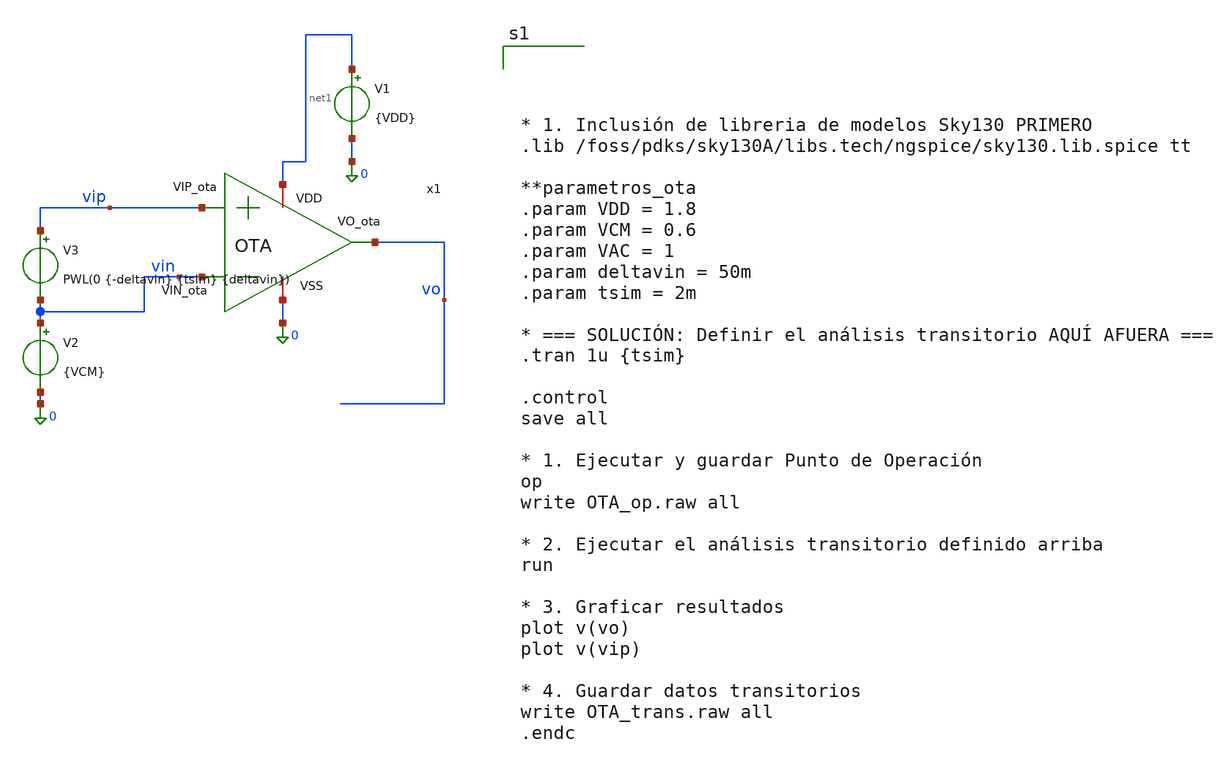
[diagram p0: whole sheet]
** sch_path: xschem/OTA_tbtran.sch
**.subckt OTA_tbtran
x1 net1 vo vin vip 0 OTA
V1 net1 0 {VDD}
V2 vin 0 {VCM}
V3 vip vin PWL(0 {-deltavin} {tsim} {deltavin})
**** begin user architecture code




* 1. Inclusión de libreria de modelos Sky130 PRIMERO
.lib /foss/pdks/sky130A/libs.tech/ngspice/sky130.lib.spice tt

**parametros_ota
.param VDD = 1.8
.param VCM = 0.6
.param VAC = 1
.param deltavin = 50m
.param tsim = 2m

* === SOLUCIÓN: Definir el análisis transitorio AQUÍ AFUERA ===
.tran 1u {tsim}

.control
save all

* 1. Ejecutar y guardar Punto de Operación
op
write OTA_op.raw all

* 2. Ejecutar el análisis transitorio definido arriba
run

* 3. Graficar resultados
plot v(vo)
plot v(vip)

* 4. Guardar datos transitorios
write OTA_trans.raw all
.endc



**** end user architecture code
**.ends

* expanding   symbol:  /foss/designs/LDO-sky130/xschem/OTA.sym # of pins=5
** sym_path: xschem/OTA.sym
** sch_path: xschem/OTA.sch
.subckt OTA VDD VO_ota VIN_ota VIP_ota VSS
*.ipin VIN_ota
*.opin VO_ota
*.iopin VSS
*.iopin VDD
*.ipin VIP_ota
XR1 VO_ota1 net1 VDD sky130_fd_pr__res_high_po W=0.35 L=360 mult=1 m=1
XC1 VO_ota net1 sky130_fd_pr__cap_mim_m3_2 W=50 L=50 MF=1 m=1
XMpr VO_ota1 vd VSS VSS sky130_fd_pr__nfet_01v8 L=0.5 W=3 nf=1 ad='int((1 + 1)/2) * 3 / 1 * 0.29' as='int((1 + 2)/2) * 3 / 1 * 0.29'
+ pd='2*int((1 + 1)/2) * (3 / 1 + 0.29)' ps='2*int((1 + 2)/2) * (3 / 1 + 0.29)' nrd='0.29 / 3 ' nrs='0.29 / 3 '
+ sa=0 sb=0 sd=0 mult=1 m=1
XMnr vd vd VSS VSS sky130_fd_pr__nfet_01v8 L=0.5 W=3 nf=1 ad='int((1 + 1)/2) * 3 / 1 * 0.29' as='int((1 + 2)/2) * 3 / 1 * 0.29'
+ pd='2*int((1 + 1)/2) * (3 / 1 + 0.29)' ps='2*int((1 + 2)/2) * (3 / 1 + 0.29)' nrd='0.29 / 3 ' nrs='0.29 / 3 '
+ sa=0 sb=0 sd=0 mult=1 m=1
XMn vd VIN_ota Vtail VDD sky130_fd_pr__pfet_01v8 L=0.5 W=28 nf=1 ad='int((1 + 1)/2) * 28 / 1 * 0.29'
+ as='int((1 + 2)/2) * 28 / 1 * 0.29' pd='2*int((1 + 1)/2) * (28 / 1 + 0.29)' ps='2*int((1 + 2)/2) * (28 / 1 + 0.29)'
+ nrd='0.29 / 28 ' nrs='0.29 / 28 ' sa=0 sb=0 sd=0 mult=1 m=1
XMp VO_ota1 VIP_ota Vtail VDD sky130_fd_pr__pfet_01v8 L=0.5 W=28 nf=1 ad='int((1 + 1)/2) * 28 / 1 * 0.29'
+ as='int((1 + 2)/2) * 28 / 1 * 0.29' pd='2*int((1 + 1)/2) * (28 / 1 + 0.29)' ps='2*int((1 + 2)/2) * (28 / 1 + 0.29)'
+ nrd='0.29 / 28 ' nrs='0.29 / 28 ' sa=0 sb=0 sd=0 mult=1 m=1
XMo VO_ota VO_ota1 VSS VSS sky130_fd_pr__nfet_01v8 L=0.5 W=3 nf=1 ad='int((1 + 1)/2) * 3 / 1 * 0.29'
+ as='int((1 + 2)/2) * 3 / 1 * 0.29' pd='2*int((1 + 1)/2) * (3 / 1 + 0.29)' ps='2*int((1 + 2)/2) * (3 / 1 + 0.29)'
+ nrd='0.29 / 3 ' nrs='0.29 / 3 ' sa=0 sb=0 sd=0 mult=1 m=1
XMrc1 Vtail VGP VDD VDD sky130_fd_pr__pfet_01v8_lvt L=0.5 W=40 nf=1 ad='int((1 + 1)/2) * 40 / 1 * 0.29'
+ as='int((1 + 2)/2) * 40 / 1 * 0.29' pd='2*int((1 + 1)/2) * (40 / 1 + 0.29)' ps='2*int((1 + 2)/2) * (40 / 1 + 0.29)'
+ nrd='0.29 / 40 ' nrs='0.29 / 40 ' sa=0 sb=0 sd=0 mult=1 m=1
XMrc2 VO_ota VGP VDD VDD sky130_fd_pr__pfet_01v8_lvt L=0.5 W=8 nf=1 ad='int((1 + 1)/2) * 8 / 1 * 0.29'
+ as='int((1 + 2)/2) * 8 / 1 * 0.29' pd='2*int((1 + 1)/2) * (8 / 1 + 0.29)' ps='2*int((1 + 2)/2) * (8 / 1 + 0.29)'
+ nrd='0.29 / 8 ' nrs='0.29 / 8 ' sa=0 sb=0 sd=0 mult=1 m=1
XMc3 VGP Viref rs VSS sky130_fd_pr__nfet_01v8 L=1 W=20 nf=1 ad='int((1 + 1)/2) * 20 / 1 * 0.29' as='int((1 + 2)/2) * 20 / 1 * 0.29'
+ pd='2*int((1 + 1)/2) * (20 / 1 + 0.29)' ps='2*int((1 + 2)/2) * (20 / 1 + 0.29)' nrd='0.29 / 20 ' nrs='0.29 / 20 '
+ sa=0 sb=0 sd=0 mult=1 m=1
XMp2 Viref Viref VSS VSS sky130_fd_pr__nfet_01v8 L=1 W=5 nf=1 ad='int((1 + 1)/2) * 5 / 1 * 0.29' as='int((1 + 2)/2) * 5 / 1 * 0.29'
+ pd='2*int((1 + 1)/2) * (5 / 1 + 0.29)' ps='2*int((1 + 2)/2) * (5 / 1 + 0.29)' nrd='0.29 / 5 ' nrs='0.29 / 5 '
+ sa=0 sb=0 sd=0 mult=1 m=1
XMr VGP VGP VDD VDD sky130_fd_pr__pfet_01v8_lvt L=0.5 W=2.4 nf=1 ad='int((1 + 1)/2) * 2.4 / 1 * 0.29'
+ as='int((1 + 2)/2) * 2.4 / 1 * 0.29' pd='2*int((1 + 1)/2) * (2.4 / 1 + 0.29)' ps='2*int((1 + 2)/2) * (2.4 / 1 + 0.29)'
+ nrd='0.29 / 2.4 ' nrs='0.29 / 2.4 ' sa=0 sb=0 sd=0 mult=1 m=1
XMr1 Viref VGP VDD VDD sky130_fd_pr__pfet_01v8_lvt L=1 W=8 nf=1 ad='int((1 + 1)/2) * 8 / 1 * 0.29' as='int((1 + 2)/2) * 8 / 1 * 0.29'
+ pd='2*int((1 + 1)/2) * (8 / 1 + 0.29)' ps='2*int((1 + 2)/2) * (8 / 1 + 0.29)' nrd='0.29 / 8 ' nrs='0.29 / 8 '
+ sa=0 sb=0 sd=0 mult=1 m=1
XRs VSS rs VSS sky130_fd_pr__res_iso_pw W=0.425 L=0.35 m=1
.ends

.end
